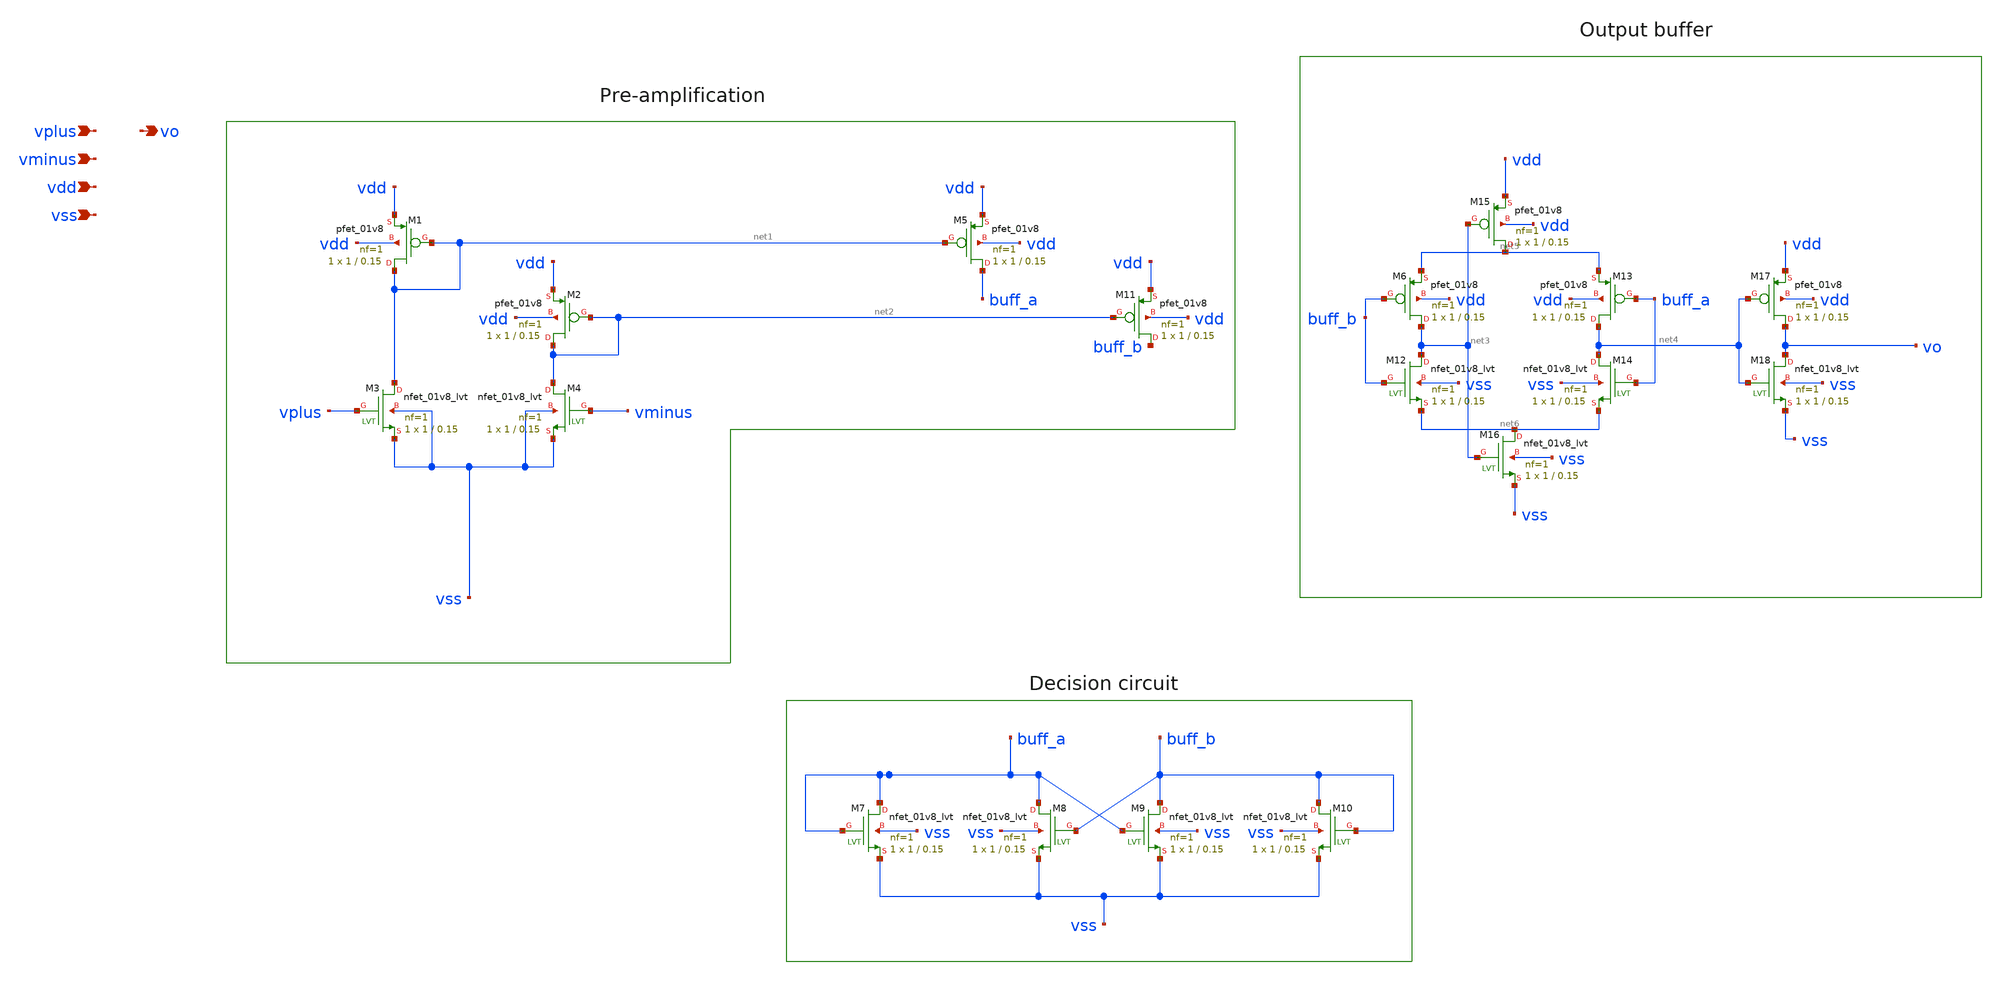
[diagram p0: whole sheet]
** sch_path: comparator2_copy.sch
**.subckt comparator2_copy vplus vminus vdd vss vo
*.ipin vplus
*.ipin vminus
*.ipin vdd
*.ipin vss
*.opin vo
XM1 net1 net1 vdd vdd sky130_fd_pr__pfet_01v8 L=0.15 W=1 nf=1 ad='int((1 + 1)/2) * 1 / 1 * 0.29' as='int((1 + 2)/2) * 1 / 1 * 0.29'
+ pd='2*int((1 + 1)/2) * (1 / 1 + 0.29)' ps='2*int((1 + 2)/2) * (1 / 1 + 0.29)' nrd='0.29 / 1 ' nrs='0.29 / 1 '
+ sa=0 sb=0 sd=0 mult=1 m=1
XM2 net2 net2 vdd vdd sky130_fd_pr__pfet_01v8 L=0.15 W=1 nf=1 ad='int((1 + 1)/2) * 1 / 1 * 0.29' as='int((1 + 2)/2) * 1 / 1 * 0.29'
+ pd='2*int((1 + 1)/2) * (1 / 1 + 0.29)' ps='2*int((1 + 2)/2) * (1 / 1 + 0.29)' nrd='0.29 / 1 ' nrs='0.29 / 1 '
+ sa=0 sb=0 sd=0 mult=1 m=1
XM3 net1 vplus vss vss sky130_fd_pr__nfet_01v8_lvt L=0.15 W=1 nf=1 ad='int((1 + 1)/2) * 1 / 1 * 0.29'
+ as='int((1 + 2)/2) * 1 / 1 * 0.29' pd='2*int((1 + 1)/2) * (1 / 1 + 0.29)' ps='2*int((1 + 2)/2) * (1 / 1 + 0.29)'
+ nrd='0.29 / 1 ' nrs='0.29 / 1 ' sa=0 sb=0 sd=0 mult=1 m=1
XM4 net2 vminus vss vss sky130_fd_pr__nfet_01v8_lvt L=0.15 W=1 nf=1 ad='int((1 + 1)/2) * 1 / 1 * 0.29'
+ as='int((1 + 2)/2) * 1 / 1 * 0.29' pd='2*int((1 + 1)/2) * (1 / 1 + 0.29)' ps='2*int((1 + 2)/2) * (1 / 1 + 0.29)'
+ nrd='0.29 / 1 ' nrs='0.29 / 1 ' sa=0 sb=0 sd=0 mult=1 m=1
XM5 buff_a net1 vdd vdd sky130_fd_pr__pfet_01v8 L=0.15 W=1 nf=1 ad='int((1 + 1)/2) * 1 / 1 * 0.29' as='int((1 + 2)/2) * 1 / 1 * 0.29'
+ pd='2*int((1 + 1)/2) * (1 / 1 + 0.29)' ps='2*int((1 + 2)/2) * (1 / 1 + 0.29)' nrd='0.29 / 1 ' nrs='0.29 / 1 '
+ sa=0 sb=0 sd=0 mult=1 m=1
XM7 buff_a buff_a vss vss sky130_fd_pr__nfet_01v8_lvt L=0.15 W=1 nf=1 ad='int((1 + 1)/2) * 1 / 1 * 0.29'
+ as='int((1 + 2)/2) * 1 / 1 * 0.29' pd='2*int((1 + 1)/2) * (1 / 1 + 0.29)' ps='2*int((1 + 2)/2) * (1 / 1 + 0.29)'
+ nrd='0.29 / 1 ' nrs='0.29 / 1 ' sa=0 sb=0 sd=0 mult=1 m=1
XM8 buff_a buff_b vss vss sky130_fd_pr__nfet_01v8_lvt L=0.15 W=1 nf=1 ad='int((1 + 1)/2) * 1 / 1 * 0.29'
+ as='int((1 + 2)/2) * 1 / 1 * 0.29' pd='2*int((1 + 1)/2) * (1 / 1 + 0.29)' ps='2*int((1 + 2)/2) * (1 / 1 + 0.29)'
+ nrd='0.29 / 1 ' nrs='0.29 / 1 ' sa=0 sb=0 sd=0 mult=1 m=1
XM9 buff_b buff_a vss vss sky130_fd_pr__nfet_01v8_lvt L=0.15 W=1 nf=1 ad='int((1 + 1)/2) * 1 / 1 * 0.29'
+ as='int((1 + 2)/2) * 1 / 1 * 0.29' pd='2*int((1 + 1)/2) * (1 / 1 + 0.29)' ps='2*int((1 + 2)/2) * (1 / 1 + 0.29)'
+ nrd='0.29 / 1 ' nrs='0.29 / 1 ' sa=0 sb=0 sd=0 mult=1 m=1
XM10 buff_b buff_b vss vss sky130_fd_pr__nfet_01v8_lvt L=0.15 W=1 nf=1 ad='int((1 + 1)/2) * 1 / 1 * 0.29'
+ as='int((1 + 2)/2) * 1 / 1 * 0.29' pd='2*int((1 + 1)/2) * (1 / 1 + 0.29)' ps='2*int((1 + 2)/2) * (1 / 1 + 0.29)'
+ nrd='0.29 / 1 ' nrs='0.29 / 1 ' sa=0 sb=0 sd=0 mult=1 m=1
XM11 buff_b net2 vdd vdd sky130_fd_pr__pfet_01v8 L=0.15 W=1 nf=1 ad='int((1 + 1)/2) * 1 / 1 * 0.29' as='int((1 + 2)/2) * 1 / 1 * 0.29'
+ pd='2*int((1 + 1)/2) * (1 / 1 + 0.29)' ps='2*int((1 + 2)/2) * (1 / 1 + 0.29)' nrd='0.29 / 1 ' nrs='0.29 / 1 '
+ sa=0 sb=0 sd=0 mult=1 m=1
XM6 net3 buff_b net5 vdd sky130_fd_pr__pfet_01v8 L=0.15 W=1 nf=1 ad='int((1 + 1)/2) * 1 / 1 * 0.29' as='int((1 + 2)/2) * 1 / 1 * 0.29'
+ pd='2*int((1 + 1)/2) * (1 / 1 + 0.29)' ps='2*int((1 + 2)/2) * (1 / 1 + 0.29)' nrd='0.29 / 1 ' nrs='0.29 / 1 '
+ sa=0 sb=0 sd=0 mult=1 m=1
XM12 net3 buff_b net6 vss sky130_fd_pr__nfet_01v8_lvt L=0.15 W=1 nf=1 ad='int((1 + 1)/2) * 1 / 1 * 0.29'
+ as='int((1 + 2)/2) * 1 / 1 * 0.29' pd='2*int((1 + 1)/2) * (1 / 1 + 0.29)' ps='2*int((1 + 2)/2) * (1 / 1 + 0.29)'
+ nrd='0.29 / 1 ' nrs='0.29 / 1 ' sa=0 sb=0 sd=0 mult=1 m=1
XM13 net4 buff_a net5 vdd sky130_fd_pr__pfet_01v8 L=0.15 W=1 nf=1 ad='int((1 + 1)/2) * 1 / 1 * 0.29'
+ as='int((1 + 2)/2) * 1 / 1 * 0.29' pd='2*int((1 + 1)/2) * (1 / 1 + 0.29)' ps='2*int((1 + 2)/2) * (1 / 1 + 0.29)'
+ nrd='0.29 / 1 ' nrs='0.29 / 1 ' sa=0 sb=0 sd=0 mult=1 m=1
XM14 net4 buff_a net6 vss sky130_fd_pr__nfet_01v8_lvt L=0.15 W=1 nf=1 ad='int((1 + 1)/2) * 1 / 1 * 0.29'
+ as='int((1 + 2)/2) * 1 / 1 * 0.29' pd='2*int((1 + 1)/2) * (1 / 1 + 0.29)' ps='2*int((1 + 2)/2) * (1 / 1 + 0.29)'
+ nrd='0.29 / 1 ' nrs='0.29 / 1 ' sa=0 sb=0 sd=0 mult=1 m=1
XM15 net5 net3 vdd vdd sky130_fd_pr__pfet_01v8 L=0.15 W=1 nf=1 ad='int((1 + 1)/2) * 1 / 1 * 0.29' as='int((1 + 2)/2) * 1 / 1 * 0.29'
+ pd='2*int((1 + 1)/2) * (1 / 1 + 0.29)' ps='2*int((1 + 2)/2) * (1 / 1 + 0.29)' nrd='0.29 / 1 ' nrs='0.29 / 1 '
+ sa=0 sb=0 sd=0 mult=1 m=1
XM16 net6 net3 vss vss sky130_fd_pr__nfet_01v8_lvt L=0.15 W=1 nf=1 ad='int((1 + 1)/2) * 1 / 1 * 0.29'
+ as='int((1 + 2)/2) * 1 / 1 * 0.29' pd='2*int((1 + 1)/2) * (1 / 1 + 0.29)' ps='2*int((1 + 2)/2) * (1 / 1 + 0.29)'
+ nrd='0.29 / 1 ' nrs='0.29 / 1 ' sa=0 sb=0 sd=0 mult=1 m=1
XM17 vo net4 vdd vdd sky130_fd_pr__pfet_01v8 L=0.15 W=1 nf=1 ad='int((1 + 1)/2) * 1 / 1 * 0.29' as='int((1 + 2)/2) * 1 / 1 * 0.29'
+ pd='2*int((1 + 1)/2) * (1 / 1 + 0.29)' ps='2*int((1 + 2)/2) * (1 / 1 + 0.29)' nrd='0.29 / 1 ' nrs='0.29 / 1 '
+ sa=0 sb=0 sd=0 mult=1 m=1
XM18 vo net4 vss vss sky130_fd_pr__nfet_01v8_lvt L=0.15 W=1 nf=1 ad='int((1 + 1)/2) * 1 / 1 * 0.29' as='int((1 + 2)/2) * 1 / 1 * 0.29'
+ pd='2*int((1 + 1)/2) * (1 / 1 + 0.29)' ps='2*int((1 + 2)/2) * (1 / 1 + 0.29)' nrd='0.29 / 1 ' nrs='0.29 / 1 '
+ sa=0 sb=0 sd=0 mult=1 m=1
**.ends
.end
